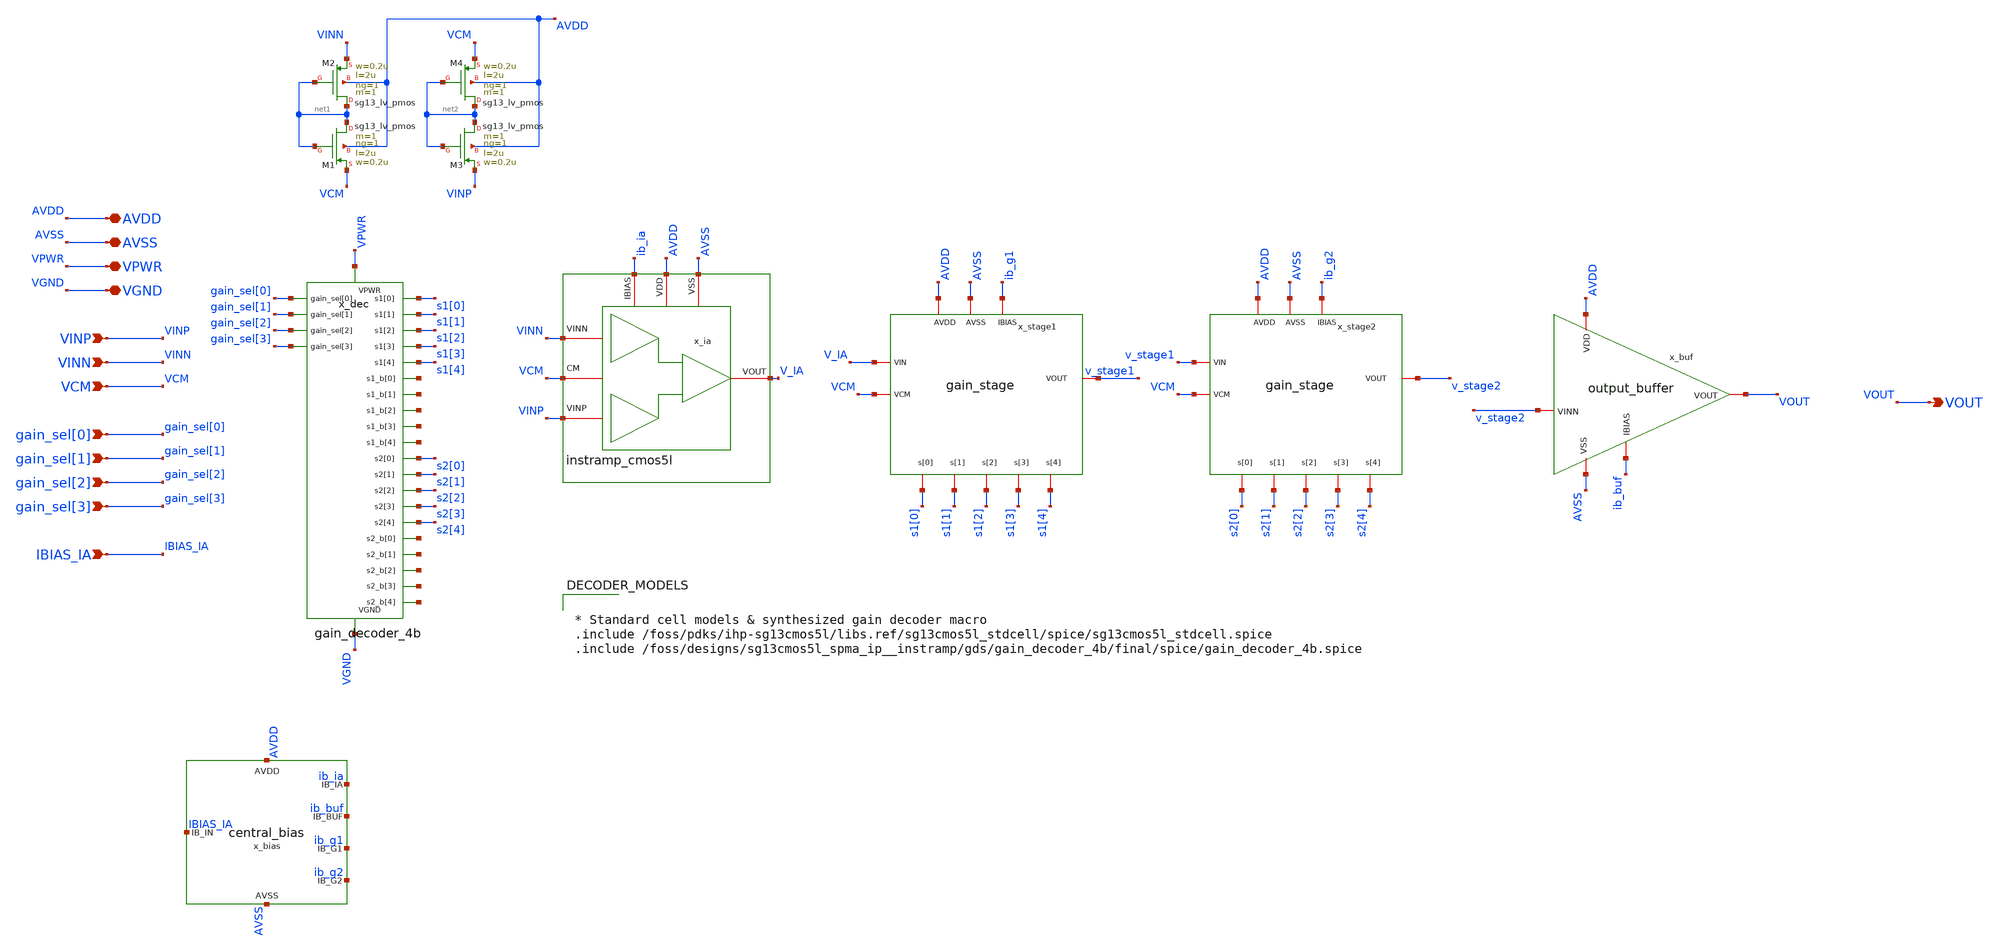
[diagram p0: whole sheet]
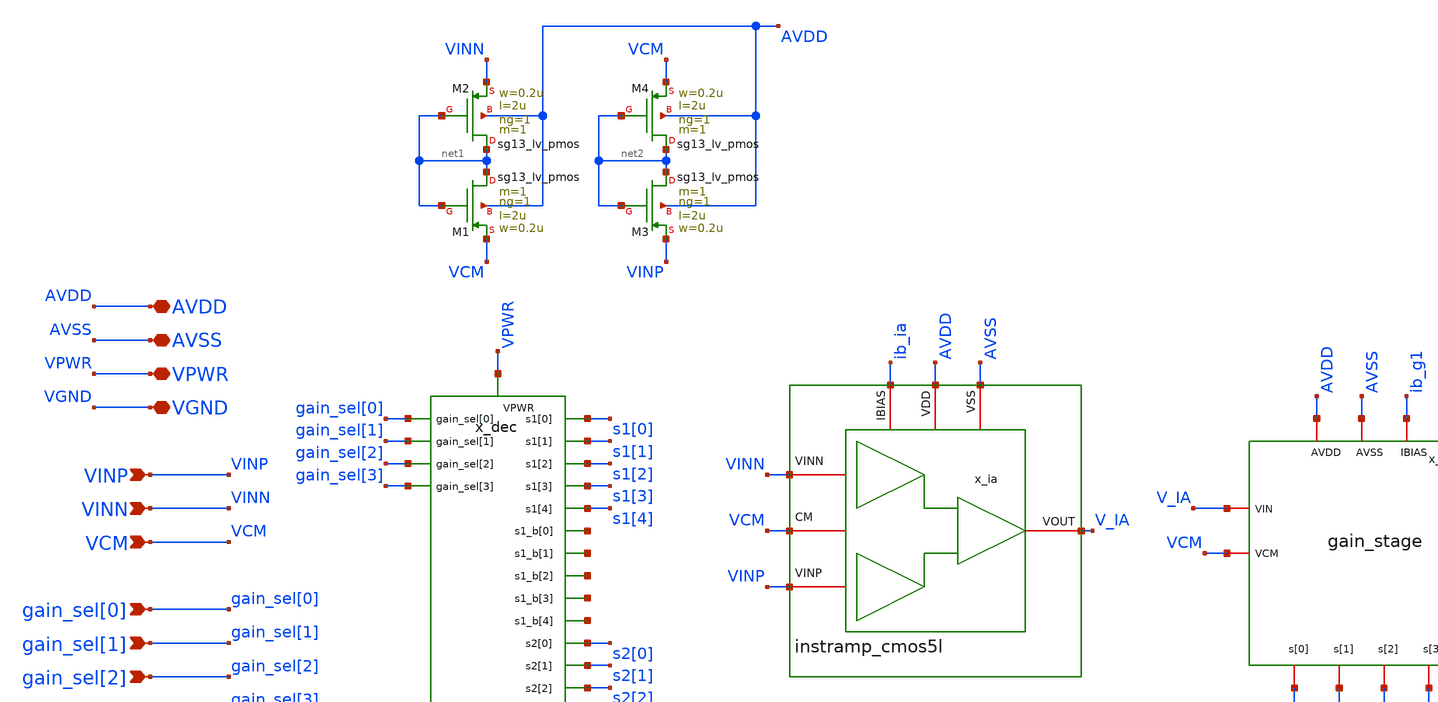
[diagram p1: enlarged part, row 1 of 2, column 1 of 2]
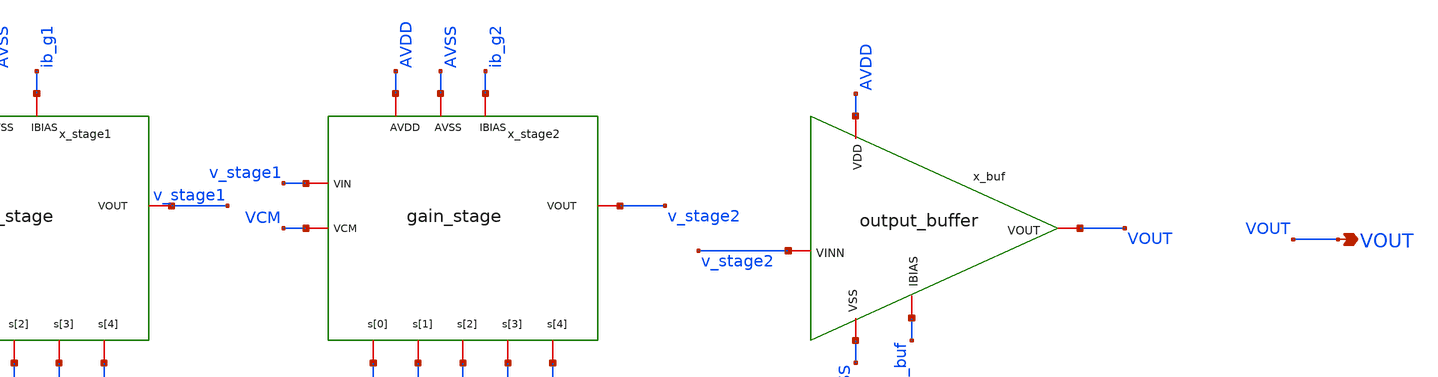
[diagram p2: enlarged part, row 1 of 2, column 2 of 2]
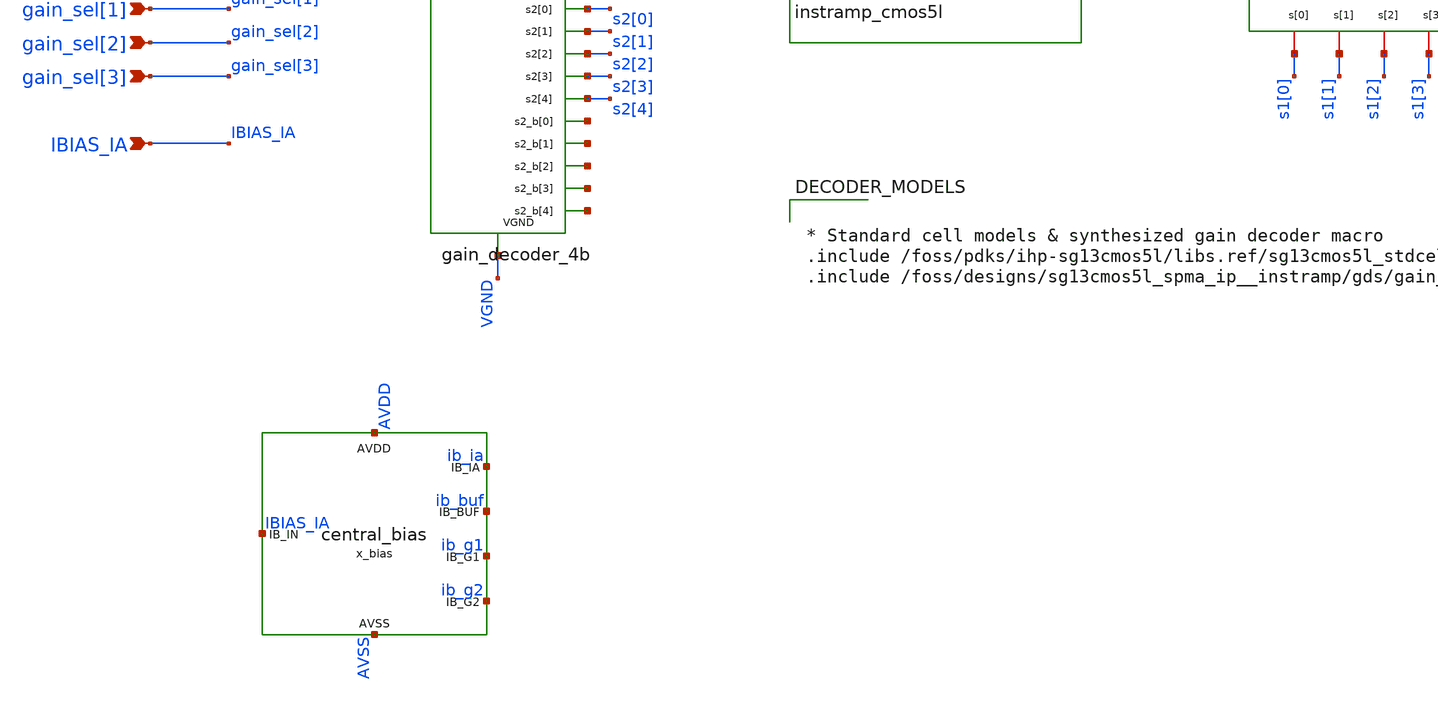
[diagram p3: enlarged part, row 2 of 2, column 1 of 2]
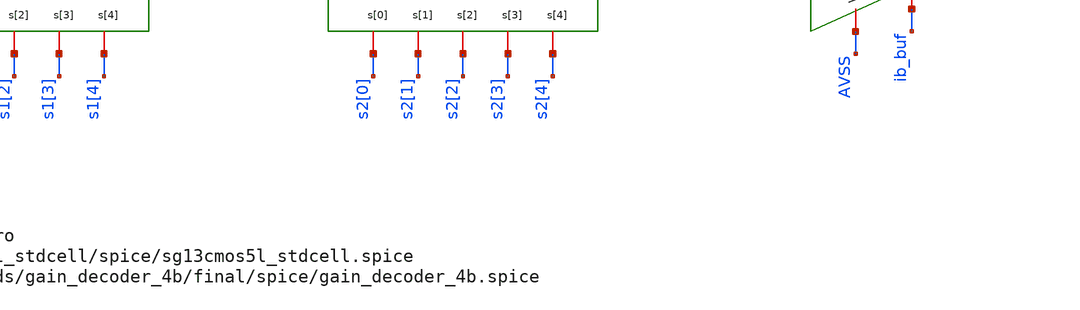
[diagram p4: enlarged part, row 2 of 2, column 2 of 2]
** sch_path: xschem/pgia_top/pgia_top.sch
**.subckt pgia_top AVDD AVSS VPWR VGND VINP VINN VCM gain_sel[0] gain_sel[1] gain_sel[2] gain_sel[3]
*+ IBIAS_IA VOUT
*.iopin AVDD
*.iopin AVSS
*.iopin VPWR
*.iopin VGND
*.ipin VINP
*.ipin VINN
*.ipin VCM
*.ipin gain_sel[0]
*.ipin gain_sel[1]
*.ipin gain_sel[2]
*.ipin gain_sel[3]
*.ipin IBIAS_IA
*.opin VOUT
x_dec VGND VPWR gain_sel[0] gain_sel[1] gain_sel[2] gain_sel[3] s1[0] s1[1] s1[2] s1[3] s1[4] net3
+ net4 net5 net6 net7 s2[0] s2[1] s2[2] s2[3] s2[4] net8 net9 net10 net11 net12 gain_decoder_4b
x_ia AVSS AVDD ib_ia VINN V_IA VINP VCM instramp_cmos5l
x_stage1 AVDD AVSS ib_g1 V_IA VCM v_stage1 s1[0] s1[1] s1[2] s1[3] s1[4] gain_stage
x_stage2 AVDD AVSS ib_g2 v_stage1 VCM v_stage2 s2[0] s2[1] s2[2] s2[3] s2[4] gain_stage
x_buf AVDD AVSS ib_buf v_stage2 VOUT output_buffer
x_bias IBIAS_IA ib_ia ib_buf ib_g1 ib_g2 AVDD AVSS central_bias
XM1 net1 net1 VCM AVDD sg13_lv_pmos w=0.2u l=2u ng=1 m=1 mm_ok=1
XM2 net1 net1 VINN AVDD sg13_lv_pmos w=0.2u l=2u ng=1 m=1 mm_ok=1
XM3 net2 net2 VINP AVDD sg13_lv_pmos w=0.2u l=2u ng=1 m=1 mm_ok=1
XM4 net2 net2 VCM AVDD sg13_lv_pmos w=0.2u l=2u ng=1 m=1 mm_ok=1
**** begin user architecture code


* Standard cell models & synthesized gain decoder macro
.include /foss/pdks/ihp-sg13cmos5l/libs.ref/sg13cmos5l_stdcell/spice/sg13cmos5l_stdcell.spice
.include /foss/designs/sg13cmos5l_spma_ip__instramp/gds/gain_decoder_4b/final/spice/gain_decoder_4b.spice


**** end user architecture code
**.ends
.end
